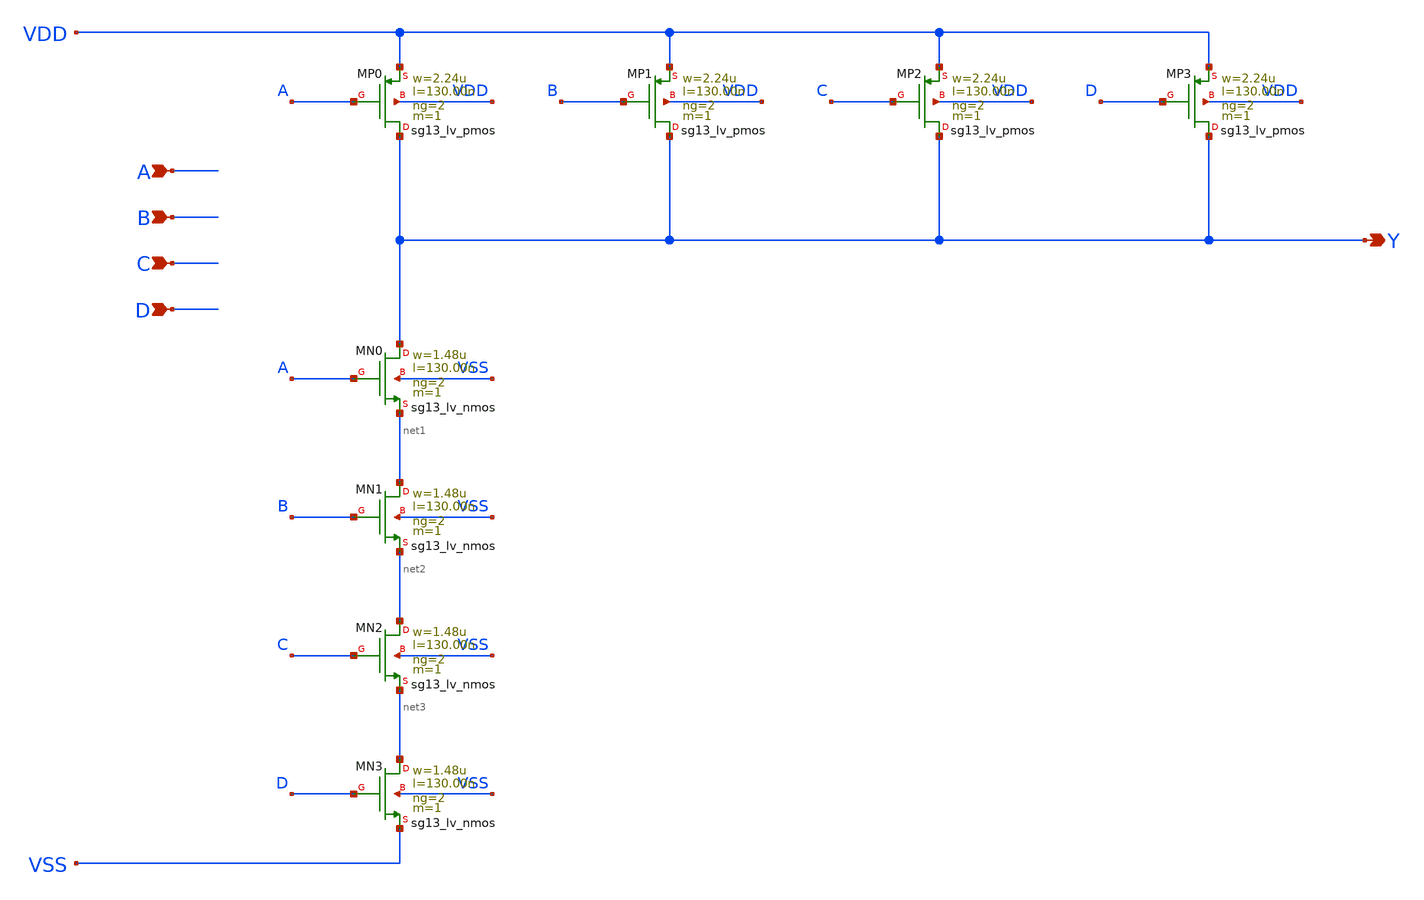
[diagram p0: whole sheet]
** sch_path: outputs/sg13g2_cells/cells/sg13g2_nand4_2/sg13g2_nand4_2.sch
**.subckt sg13g2_nand4_2 A B C D Y
*.ipin A
*.ipin B
*.ipin C
*.ipin D
*.opin Y
XMN3 net3 D VSS VSS sg13_lv_nmos w=1.48u l=130.00n ng=2 m=1 mm_ok=1
XMN1 net1 B net2 VSS sg13_lv_nmos w=1.48u l=130.00n ng=2 m=1 mm_ok=1
XMN2 net2 C net3 VSS sg13_lv_nmos w=1.48u l=130.00n ng=2 m=1 mm_ok=1
XMN0 Y A net1 VSS sg13_lv_nmos w=1.48u l=130.00n ng=2 m=1 mm_ok=1
XMP3 Y D VDD VDD sg13_lv_pmos w=2.24u l=130.00n ng=2 m=1 mm_ok=1
XMP0 Y A VDD VDD sg13_lv_pmos w=2.24u l=130.00n ng=2 m=1 mm_ok=1
XMP1 Y B VDD VDD sg13_lv_pmos w=2.24u l=130.00n ng=2 m=1 mm_ok=1
XMP2 Y C VDD VDD sg13_lv_pmos w=2.24u l=130.00n ng=2 m=1 mm_ok=1
**.ends
.end
